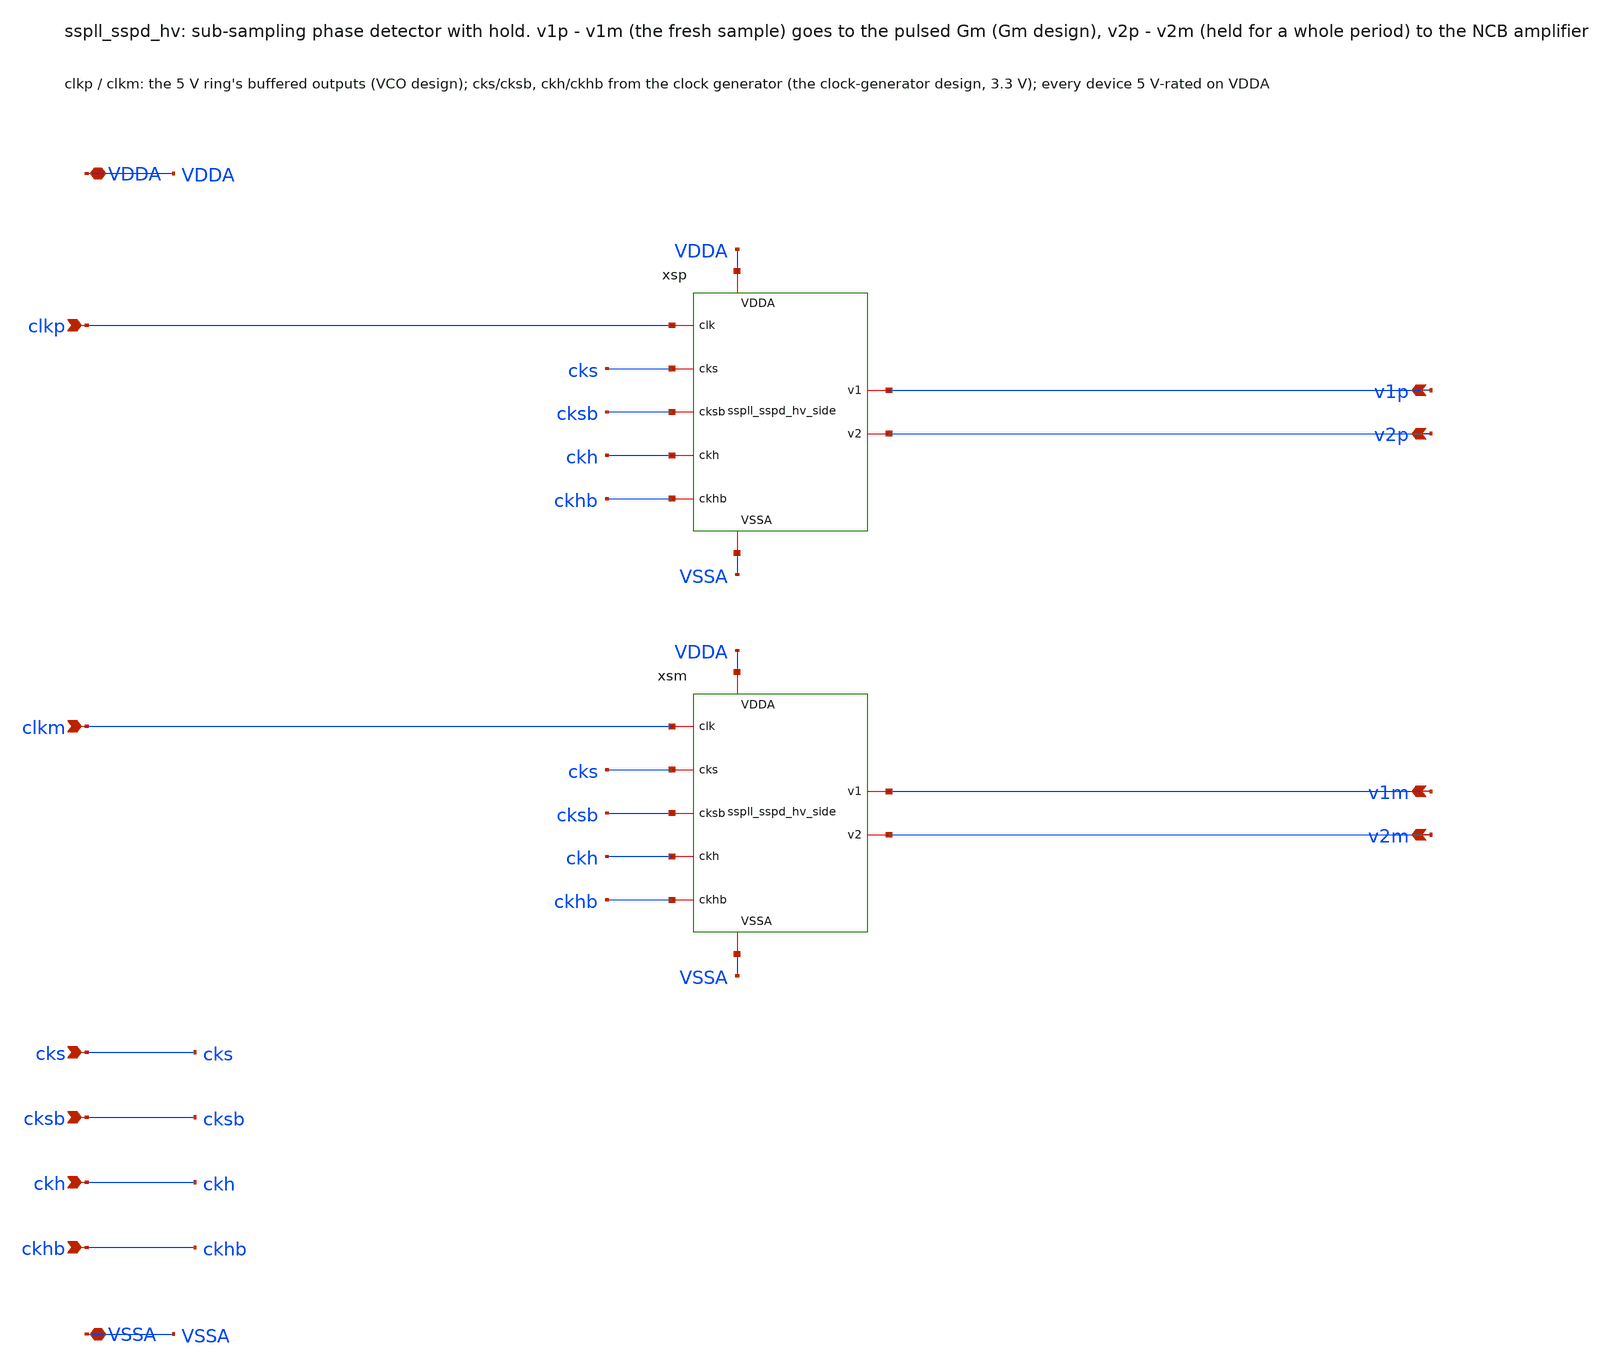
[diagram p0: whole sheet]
** sch_path: xschem/sspd_hv/sspll_sspd_hv.sch
**.subckt sspll_sspd_hv clkp clkm v1p v2p v1m v2m cks cksb ckh ckhb VDDA VSSA
*.ipin clkp
*.ipin clkm
*.opin v1p
*.opin v2p
*.opin v1m
*.opin v2m
*.ipin cks
*.ipin cksb
*.ipin ckh
*.ipin ckhb
*.iopin VDDA
*.iopin VSSA
xsp clkp cks cksb ckh ckhb v1p v2p VDDA VSSA sspll_sspd_hv_side
xsm clkm cks cksb ckh ckhb v1m v2m VDDA VSSA sspll_sspd_hv_side
**.ends
.end
